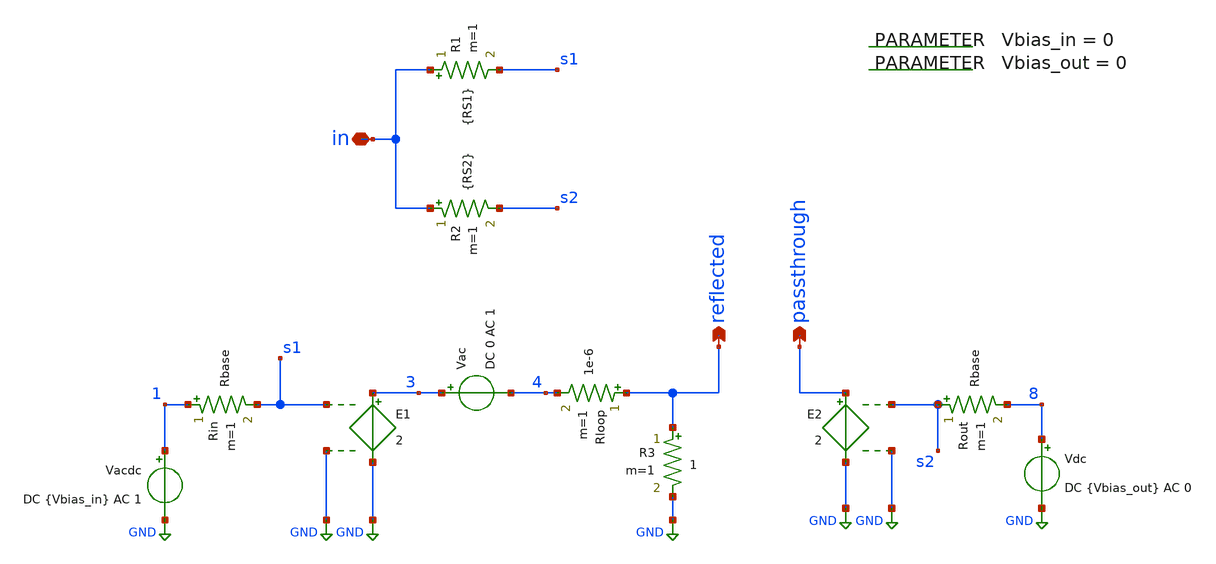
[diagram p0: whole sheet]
** sch_path: sparam/s_port.sch
**.subckt s_port in reflected passthrough
*.iopin in
*.opin reflected
*.opin passthrough
Rout s2 8 Rbase m=1
Vdc 8 GND DC {Vbias_out} AC 0
E2 passthrough GND s2 GND 2
Vacdc 1 GND DC {Vbias_in} AC 1
Rin 1 s1 Rbase m=1
E1 3 GND s1 GND 2
Vac 3 4 DC 0 AC 1
Rloop reflected 4 1e-6 m=1
R3 reflected GND 1 m=1
.param Vbias_in = 0
R1 in s1 {RS1} m=1
R2 in s2 {RS2} m=1
.param Vbias_out = 0
**.ends
.GLOBAL GND
.end
